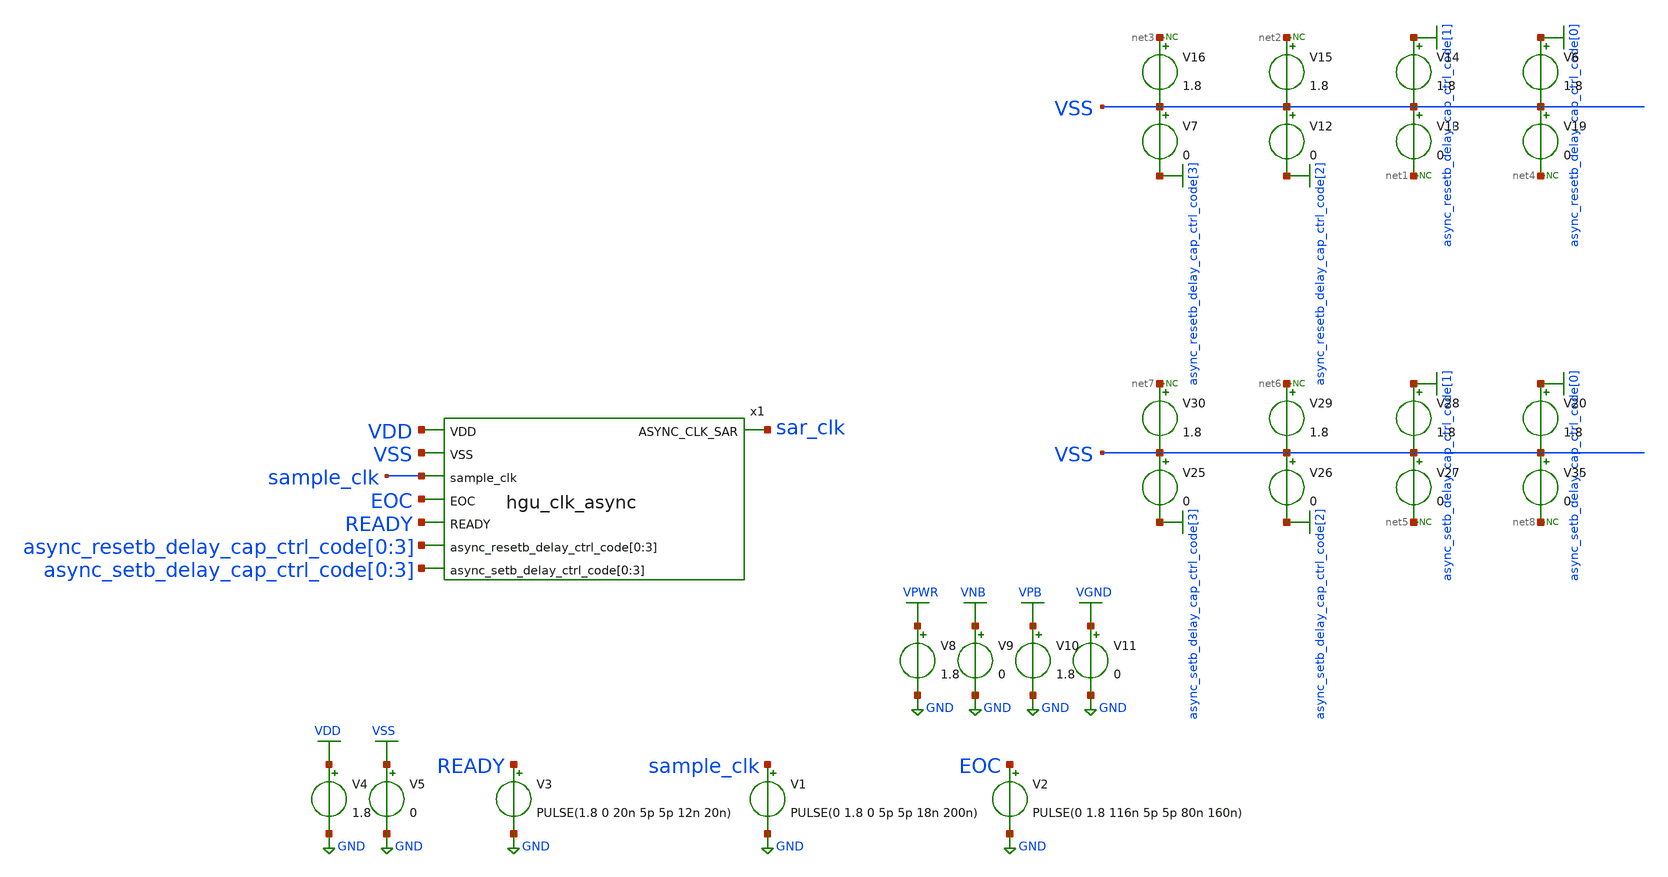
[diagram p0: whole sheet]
** sch_path: hgu/tb/tb_hgu_clk_async.sch
**.subckt tb_hgu_clk_async
V3 READY GND PULSE(1.8 0 20n 5p 5p 12n 20n)
x1 sar_clk VDD VSS sample_clk EOC READY async_resetb_delay_cap_ctrl_code[0]
+ async_resetb_delay_cap_ctrl_code[1] async_resetb_delay_cap_ctrl_code[2] async_resetb_delay_cap_ctrl_code[3]
+ async_setb_delay_cap_ctrl_code[0] async_setb_delay_cap_ctrl_code[1] async_setb_delay_cap_ctrl_code[2]
+ async_setb_delay_cap_ctrl_code[3] hgu_clk_async
V4 VDD GND 1.8
V5 VSS GND 0
V1 sample_clk GND PULSE(0 1.8 0 5p 5p 18n 200n)
V2 EOC GND PULSE(0 1.8 116n 5p 5p 80n 160n)
V8 VPWR GND 1.8
V9 VNB GND 0
V10 VPB GND 1.8
V11 VGND GND 0
V6 async_resetb_delay_cap_ctrl_code[0] VSS 1.8
V7 VSS async_resetb_delay_cap_ctrl_code[3] 0
V12 VSS async_resetb_delay_cap_ctrl_code[2] 0
V13 VSS net1 0
V14 async_resetb_delay_cap_ctrl_code[1] VSS 1.8
V15 net2 VSS 1.8
V16 net3 VSS 1.8
V19 VSS net4 0
* noconn #net3
* noconn #net2
* noconn #net1
* noconn #net4
V20 async_setb_delay_cap_ctrl_code[0] VSS 1.8
V25 VSS async_setb_delay_cap_ctrl_code[3] 0
V26 VSS async_setb_delay_cap_ctrl_code[2] 0
V27 VSS net5 0
V28 async_setb_delay_cap_ctrl_code[1] VSS 1.8
V29 net6 VSS 1.8
V30 net7 VSS 1.8
V35 VSS net8 0
* noconn #net7
* noconn #net6
* noconn #net5
* noconn #net8
**** begin user architecture code



.lib /foss/pdks/sky130A/libs.tech/ngspice/sky130.lib.spice ss
.include /foss/pdks/sky130A/libs.ref/sky130_fd_sc_hd/spice/sky130_fd_sc_hd.spice


.tran 10ps 150ns

.control
	option temp = 100
	let vdd_act = 1.62

	alter V1 vdd_act

	run
	plot V(READY)-2 V(sample_clk) V(EOC)+2 V(sar_clk)+4 V(sar_clk)-2 V(sar_clk)

        let l_vdd = vdd_act * 0.2
        let h_vdd = vdd_act * 0.8
        let m_vdd = vdd_act * 0.5
        meas tran rising_s find time when V(sar_clk)=l_vdd RISE=1 TD=10n
        meas tran rising_e find time when V(sar_clk)=h_vdd RISE=1 TD=10n
        let rising_time = rising_e-rising_s
        meas tran falling_s find time when V(sar_clk)=h_vdd FALL=1 TD=10n
        meas tran falling_e find time when V(sar_clk)=l_vdd FALL=1 TD=10n
        let falling_time = falling_e-falling_s
        meas tran IN find time when V(sample_clk)=m_vdd FALL=1 TD=10n
        meas tran OUT find time when V(sar_clk)=m_vdd RISE=1 TD=10n
        let rising_delay_1 = OUT-IN
        meas tran IN find time when V(ready)=m_vdd RISE=1 TD=24n
        meas tran OUT find time when V(sar_clk)=m_vdd RISE=1 TD=24n
        let rising_delay_2 = OUT-IN

	print rising_time falling_time rising_delay_1 rising_delay_2

 .endc
.save all



**** end user architecture code
**.ends

* expanding   symbol:  ../xschem/hgu_clk_async.sym # of pins=8
** sym_path: hgu/xschem/hgu_clk_async.sym
** sch_path: hgu/xschem/hgu_clk_async.sch
.subckt hgu_clk_async ASYNC_CLK_SAR VDD VSS sample_clk EOC READY async_resetb_delay_ctrl_code[0]
+ async_resetb_delay_ctrl_code[1] async_resetb_delay_ctrl_code[2] async_resetb_delay_ctrl_code[3] async_setb_delay_ctrl_code[0]
+ async_setb_delay_ctrl_code[1] async_setb_delay_ctrl_code[2] async_setb_delay_ctrl_code[3]
*.ipin VDD
*.opin ASYNC_CLK_SAR
*.ipin VSS
*.ipin sample_clk
*.ipin EOC
*.ipin READY
*.ipin
*+ async_resetb_delay_ctrl_code[0],async_resetb_delay_ctrl_code[1],async_resetb_delay_ctrl_code[2],async_resetb_delay_ctrl_code[3]
*.ipin
*+ async_setb_delay_ctrl_code[0],async_setb_delay_ctrl_code[1],async_setb_delay_ctrl_code[2],async_setb_delay_ctrl_code[3]
x3 net2 VSS sample_clk VGND VNB VPB VPWR net4 sky130_fd_sc_hd__mux2_1
x8 net4 VSS EOC VGND VNB VPB VPWR ASYNC_CLK_SAR sky130_fd_sc_hd__mux2_1
x27 sample_clk VDD net5 net6 VGND VNB VPB VPWR net2 net7 sky130_fd_sc_hd__dfbbp_1
x9 net1 VGND VNB VPB VPWR net6 sky130_fd_sc_hd__inv_1
x10 net3 VGND VNB VPB VPWR net5 sky130_fd_sc_hd__inv_1
* noconn #net7
C3 net2 VSS 5f m=1
C4 net4 VSS 5f m=1
x2 VDD READY net1 VSS async_setb_delay_ctrl_code[0] async_setb_delay_ctrl_code[1]
+ async_setb_delay_ctrl_code[2] async_setb_delay_ctrl_code[3] hgu_delay_no_code
x4 VDD ASYNC_CLK_SAR net3 VSS async_resetb_delay_ctrl_code[0] async_resetb_delay_ctrl_code[1]
+ async_resetb_delay_ctrl_code[2] async_resetb_delay_ctrl_code[3] hgu_delay_no_code
C1 net3 VSS 5f m=1
C2 net1 VSS 5f m=1
.ends


* expanding   symbol:  ../xschem/hgu_delay_no_code.sym # of pins=5
** sym_path: hgu/xschem/hgu_delay_no_code.sym
** sch_path: hgu/xschem/hgu_delay_no_code.sch
.subckt hgu_delay_no_code VDD IN OUT VSS code[0] code[1] code[2] code[3]
*.ipin IN
*.ipin VDD
*.ipin VSS
*.opin OUT
*.ipin code[0],code[1],code[2],code[3]
XM13 OUT Uc net2 VSS sky130_fd_pr__nfet_01v8 L=0.15 W=0.8 nf=1 ad='int((nf+1)/2) * W/nf * 0.29' as='int((nf+2)/2) * W/nf * 0.29'
+ pd='2*int((nf+1)/2) * (W/nf + 0.29)' ps='2*int((nf+2)/2) * (W/nf + 0.29)' nrd='0.29 / W' nrs='0.29 / W'
+ sa=0 sb=0 sd=0 mult=1 m=1
XM15 net2 Uc VSS VSS sky130_fd_pr__nfet_01v8 L=0.15 W=0.8 nf=1 ad='int((nf+1)/2) * W/nf * 0.29' as='int((nf+2)/2) * W/nf * 0.29'
+ pd='2*int((nf+1)/2) * (W/nf + 0.29)' ps='2*int((nf+2)/2) * (W/nf + 0.29)' nrd='0.29 / W' nrs='0.29 / W'
+ sa=0 sb=0 sd=0 mult=1 m=1
XM1 VDD OUT net2 VSS sky130_fd_pr__nfet_01v8 L=0.15 W='0.42 * 2 ' nf=2 ad='int((nf+1)/2) * W / nf * 0.29'
+ as='int((nf+2)/2) * W / nf * 0.29' pd='2*int((nf+1)/2) * (W / nf + 0.29)' ps='2*int((nf+2)/2) * (W / nf + 0.29)'
+ nrd='0.29 / W ' nrs='0.29 / W ' sa=0 sb=0 sd=0 mult=1 m=1
XM3 VDD Uc VDD VDD sky130_fd_pr__pfet_01v8 L=6 W=0.42 nf=1 ad='int((nf+1)/2) * W/nf * 0.29' as='int((nf+2)/2) * W/nf * 0.29'
+ pd='2*int((nf+1)/2) * (W/nf + 0.29)' ps='2*int((nf+2)/2) * (W/nf + 0.29)' nrd='0.29 / W' nrs='0.29 / W'
+ sa=0 sb=0 sd=0 mult=1 m=1
XM46 OUT Uc net1 VDD sky130_fd_pr__pfet_01v8_hvt L=0.15 W=0.42 nf=1 ad='int((nf+1)/2) * W/nf * 0.29'
+ as='int((nf+2)/2) * W/nf * 0.29' pd='2*int((nf+1)/2) * (W/nf + 0.29)' ps='2*int((nf+2)/2) * (W/nf + 0.29)'
+ nrd='0.29 / W' nrs='0.29 / W' sa=0 sb=0 sd=0 mult=1 m=1
XM47 net1 Uc VDD VDD sky130_fd_pr__pfet_01v8_hvt L=0.15 W=0.42 nf=1 ad='int((nf+1)/2) * W/nf * 0.29'
+ as='int((nf+2)/2) * W/nf * 0.29' pd='2*int((nf+1)/2) * (W/nf + 0.29)' ps='2*int((nf+2)/2) * (W/nf + 0.29)'
+ nrd='0.29 / W' nrs='0.29 / W' sa=0 sb=0 sd=0 mult=1 m=1
XM48 VSS OUT net1 VDD sky130_fd_pr__pfet_01v8_hvt L=0.15 W='0.42 * 2 ' nf=2 ad='int((nf+1)/2) * W / nf * 0.29'
+ as='int((nf+2)/2) * W / nf * 0.29' pd='2*int((nf+1)/2) * (W / nf + 0.29)' ps='2*int((nf+2)/2) * (W / nf + 0.29)'
+ nrd='0.29 / W ' nrs='0.29 / W ' sa=0 sb=0 sd=0 mult=1 m=1
x2 code[0] VSS Uc hgu_sw_cap DELAY_CAP=5f
x3[1] code[1] VSS Uc hgu_sw_cap DELAY_CAP=5f
x3[0] code[1] VSS Uc hgu_sw_cap DELAY_CAP=5f
x4[3] code[2] VSS Uc hgu_sw_cap DELAY_CAP=5f
x4[2] code[2] VSS Uc hgu_sw_cap DELAY_CAP=5f
x4[1] code[2] VSS Uc hgu_sw_cap DELAY_CAP=5f
x4[0] code[2] VSS Uc hgu_sw_cap DELAY_CAP=5f
x5[7] code[3] Uc VDD VSS hgu_sw_cap_pmos
x5[6] code[3] Uc VDD VSS hgu_sw_cap_pmos
x5[5] code[3] Uc VDD VSS hgu_sw_cap_pmos
x5[4] code[3] Uc VDD VSS hgu_sw_cap_pmos
x5[3] code[3] Uc VDD VSS hgu_sw_cap_pmos
x5[2] code[3] Uc VDD VSS hgu_sw_cap_pmos
x5[1] code[3] Uc VDD VSS hgu_sw_cap_pmos
x5[0] code[3] Uc VDD VSS hgu_sw_cap_pmos
x3 VDD IN Uc hgu_pfet_hvt_stack_in_delay
x4 IN Uc VSS hgu_nfet_hvt_stack_in_delay
.ends


* expanding   symbol:  /foss/designs/hgu_goss/hgu/xschem/hgu_sw_cap.sym # of pins=3
** sym_path: hgu/xschem/hgu_sw_cap.sym
** sch_path: hgu/xschem/hgu_sw_cap.sch
.subckt hgu_sw_cap SW VSS DELAY_SIGNAL  DELAY_CAP=DELAY_CAP
*.ipin SW
*.ipin VSS
*.iopin DELAY_SIGNAL
XM14 DELAY_SIGNAL SW net1 VSS sky130_fd_pr__nfet_01v8 L=0.15 W=0.42 nf=1 ad='int((nf+1)/2) * W/nf * 0.29'
+ as='int((nf+2)/2) * W/nf * 0.29' pd='2*int((nf+1)/2) * (W/nf + 0.29)' ps='2*int((nf+2)/2) * (W/nf + 0.29)'
+ nrd='0.29 / W' nrs='0.29 / W' sa=0 sb=0 sd=0 mult=1 m=1
C1 net2 net3 4.37f m=1
XC2 net1 VSS VSS sky130_fd_pr__cap_vpp_02p4x04p6_m1m2_noshield mult=1 m=1
.ends


* expanding   symbol:  /foss/designs/hgu_goss/hgu/xschem/hgu_sw_cap_pmos.sym # of pins=4
** sym_path: hgu/xschem/hgu_sw_cap_pmos.sym
** sch_path: hgu/xschem/hgu_sw_cap_pmos.sch
.subckt hgu_sw_cap_pmos SW DELAY_SIGNAL VDD VSS
*.ipin SW
*.ipin VDD
*.iopin DELAY_SIGNAL
*.ipin VSS
XM16 net1 SW VDD VDD sky130_fd_pr__pfet_01v8 L=0.15 W=0.42 nf=1 ad='int((nf+1)/2) * W/nf * 0.29' as='int((nf+2)/2) * W/nf * 0.29'
+ pd='2*int((nf+1)/2) * (W/nf + 0.29)' ps='2*int((nf+2)/2) * (W/nf + 0.29)' nrd='0.29 / W' nrs='0.29 / W'
+ sa=0 sb=0 sd=0 mult=1 m=1
x1 net1 DELAY_SIGNAL VSS hgu_cdac_unit
.ends


* expanding   symbol:
*+  /foss/designs/hgu_goss/hgu/xschem/../../../hgu_goss/hgu/xschem/hgu_pfet_hvt_stack_in_delay.sym # of pins=3
** sym_path: hgu/xschem/hgu_pfet_hvt_stack_in_delay.sym
** sch_path: hgu/xschem/hgu_pfet_hvt_stack_in_delay.sch
.subckt hgu_pfet_hvt_stack_in_delay VDD input_stack output_stack
*.ipin VDD
*.ipin input_stack
*.iopin output_stack
XM1 output_stack input_stack net1 VDD sky130_fd_pr__pfet_01v8_hvt L=0.15 W=0.42 nf=1 ad='int((nf+1)/2) * W/nf * 0.29'
+ as='int((nf+2)/2) * W/nf * 0.29' pd='2*int((nf+1)/2) * (W/nf + 0.29)' ps='2*int((nf+2)/2) * (W/nf + 0.29)'
+ nrd='0.29 / W' nrs='0.29 / W' sa=0 sb=0 sd=0 mult=1 m=1
XM2 net1 input_stack net2 VDD sky130_fd_pr__pfet_01v8_hvt L=0.15 W=0.43 nf=1 ad='int((nf+1)/2) * W/nf * 0.29'
+ as='int((nf+2)/2) * W/nf * 0.29' pd='2*int((nf+1)/2) * (W/nf + 0.29)' ps='2*int((nf+2)/2) * (W/nf + 0.29)'
+ nrd='0.29 / W' nrs='0.29 / W' sa=0 sb=0 sd=0 mult=1 m=1
XM3 net2 input_stack VDD VDD sky130_fd_pr__pfet_01v8_hvt L=0.15 W=0.43 nf=1 ad='int((nf+1)/2) * W/nf * 0.29'
+ as='int((nf+2)/2) * W/nf * 0.29' pd='2*int((nf+1)/2) * (W/nf + 0.29)' ps='2*int((nf+2)/2) * (W/nf + 0.29)'
+ nrd='0.29 / W' nrs='0.29 / W' sa=0 sb=0 sd=0 mult=1 m=1
.ends


* expanding   symbol:
*+  /foss/designs/hgu_goss/hgu/xschem/../../../hgu_goss/hgu/xschem/hgu_nfet_hvt_stack_in_delay.sym # of pins=3
** sym_path: hgu/xschem/hgu_nfet_hvt_stack_in_delay.sym
** sch_path: hgu/xschem/hgu_nfet_hvt_stack_in_delay.sch
.subckt hgu_nfet_hvt_stack_in_delay input_stack output_stack VSS
*.ipin VSS
*.ipin input_stack
*.iopin output_stack
XM6 output_stack input_stack net1 VSS sky130_fd_pr__nfet_01v8 L=0.15 W=0.43 nf=1 ad='int((nf+1)/2) * W/nf * 0.29'
+ as='int((nf+2)/2) * W/nf * 0.29' pd='2*int((nf+1)/2) * (W/nf + 0.29)' ps='2*int((nf+2)/2) * (W/nf + 0.29)'
+ nrd='0.29 / W' nrs='0.29 / W' sa=0 sb=0 sd=0 mult=1 m=1
XM1 net1 input_stack net2 VSS sky130_fd_pr__nfet_01v8 L=0.15 W=0.43 nf=1 ad='int((nf+1)/2) * W/nf * 0.29'
+ as='int((nf+2)/2) * W/nf * 0.29' pd='2*int((nf+1)/2) * (W/nf + 0.29)' ps='2*int((nf+2)/2) * (W/nf + 0.29)'
+ nrd='0.29 / W' nrs='0.29 / W' sa=0 sb=0 sd=0 mult=1 m=1
XM2 net2 input_stack net3 VSS sky130_fd_pr__nfet_01v8 L=0.15 W=0.43 nf=1 ad='int((nf+1)/2) * W/nf * 0.29'
+ as='int((nf+2)/2) * W/nf * 0.29' pd='2*int((nf+1)/2) * (W/nf + 0.29)' ps='2*int((nf+2)/2) * (W/nf + 0.29)'
+ nrd='0.29 / W' nrs='0.29 / W' sa=0 sb=0 sd=0 mult=1 m=1
XM3 net3 input_stack net4 VSS sky130_fd_pr__nfet_01v8 L=0.15 W=0.43 nf=1 ad='int((nf+1)/2) * W/nf * 0.29'
+ as='int((nf+2)/2) * W/nf * 0.29' pd='2*int((nf+1)/2) * (W/nf + 0.29)' ps='2*int((nf+2)/2) * (W/nf + 0.29)'
+ nrd='0.29 / W' nrs='0.29 / W' sa=0 sb=0 sd=0 mult=1 m=1
XM4 net4 input_stack net5 VSS sky130_fd_pr__nfet_01v8 L=0.15 W=0.43 nf=1 ad='int((nf+1)/2) * W/nf * 0.29'
+ as='int((nf+2)/2) * W/nf * 0.29' pd='2*int((nf+1)/2) * (W/nf + 0.29)' ps='2*int((nf+2)/2) * (W/nf + 0.29)'
+ nrd='0.29 / W' nrs='0.29 / W' sa=0 sb=0 sd=0 mult=1 m=1
XM5 net5 input_stack net6 VSS sky130_fd_pr__nfet_01v8 L=0.15 W=0.43 nf=1 ad='int((nf+1)/2) * W/nf * 0.29'
+ as='int((nf+2)/2) * W/nf * 0.29' pd='2*int((nf+1)/2) * (W/nf + 0.29)' ps='2*int((nf+2)/2) * (W/nf + 0.29)'
+ nrd='0.29 / W' nrs='0.29 / W' sa=0 sb=0 sd=0 mult=1 m=1
XM7 net6 input_stack net7 VSS sky130_fd_pr__nfet_01v8 L=0.15 W=0.42 nf=1 ad='int((nf+1)/2) * W/nf * 0.29'
+ as='int((nf+2)/2) * W/nf * 0.29' pd='2*int((nf+1)/2) * (W/nf + 0.29)' ps='2*int((nf+2)/2) * (W/nf + 0.29)'
+ nrd='0.29 / W' nrs='0.29 / W' sa=0 sb=0 sd=0 mult=1 m=1
XM8 net7 input_stack net8 VSS sky130_fd_pr__nfet_01v8 L=0.15 W=0.42 nf=1 ad='int((nf+1)/2) * W/nf * 0.29'
+ as='int((nf+2)/2) * W/nf * 0.29' pd='2*int((nf+1)/2) * (W/nf + 0.29)' ps='2*int((nf+2)/2) * (W/nf + 0.29)'
+ nrd='0.29 / W' nrs='0.29 / W' sa=0 sb=0 sd=0 mult=1 m=1
XM9 net8 input_stack VSS VSS sky130_fd_pr__nfet_01v8 L=0.15 W=0.42 nf=1 ad='int((nf+1)/2) * W/nf * 0.29'
+ as='int((nf+2)/2) * W/nf * 0.29' pd='2*int((nf+1)/2) * (W/nf + 0.29)' ps='2*int((nf+2)/2) * (W/nf + 0.29)'
+ nrd='0.29 / W' nrs='0.29 / W' sa=0 sb=0 sd=0 mult=1 m=1
.ends

.GLOBAL GND
.GLOBAL VDD
.GLOBAL VSS
.GLOBAL VGND
.GLOBAL VNB
.GLOBAL VPB
.GLOBAL VPWR
.GLOBAL async_resetb_delay_cap_ctrl_code[3]
.GLOBAL async_resetb_delay_cap_ctrl_code[2]
.GLOBAL async_resetb_delay_cap_ctrl_code[1]
.GLOBAL async_resetb_delay_cap_ctrl_code[0]
.GLOBAL async_setb_delay_cap_ctrl_code[3]
.GLOBAL async_setb_delay_cap_ctrl_code[2]
.GLOBAL async_setb_delay_cap_ctrl_code[1]
.GLOBAL async_setb_delay_cap_ctrl_code[0]
.end
